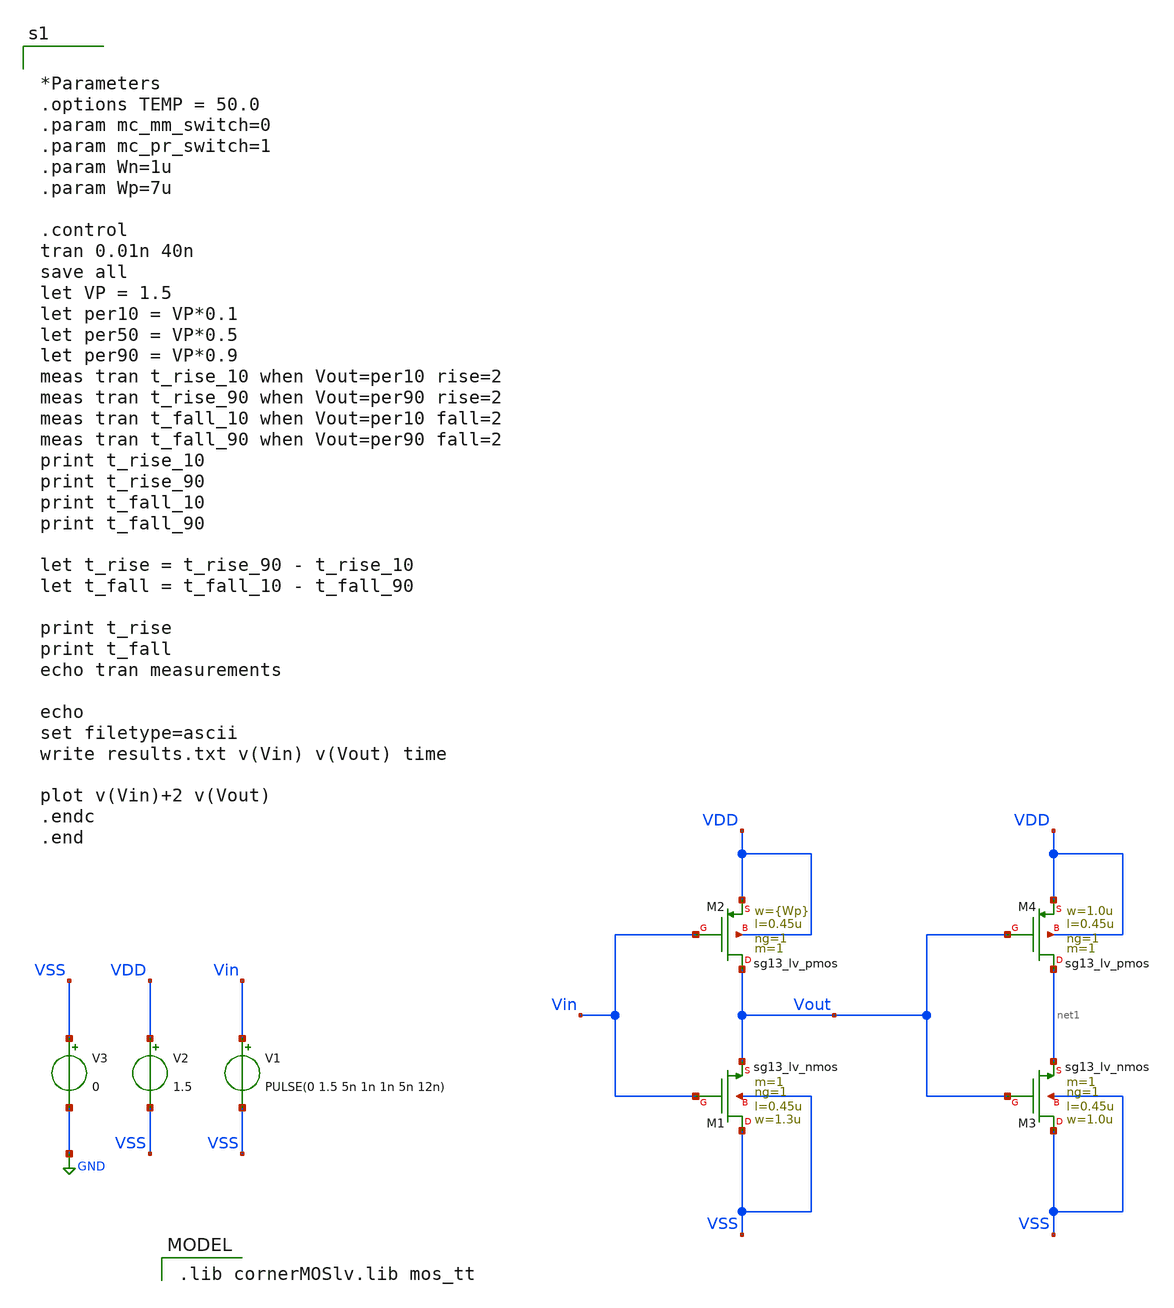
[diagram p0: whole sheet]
** sch_path: unic_cass_wrapper_user_project/ROs_reliability/inv_char.sch
**.subckt inv_char
XM1 VSS Vin Vout VSS sg13_lv_nmos w=1.3u l=0.45u ng=1 m=1 mm_ok=1
XM2 Vout Vin VDD VDD sg13_lv_pmos w={Wp} l=0.45u ng=1 m=1 mm_ok=1
XM3 VSS Vout net1 VSS sg13_lv_nmos w=1.0u l=0.45u ng=1 m=1 mm_ok=1
XM4 net1 Vout VDD VDD sg13_lv_pmos w=1.0u l=0.45u ng=1 m=1 mm_ok=1
V1 Vin VSS PULSE(0 1.5 5n 1n 1n 5n 12n)
V2 VDD VSS 1.5
V3 VSS GND 0
**** begin user architecture code
 .lib cornerMOSlv.lib mos_tt



*Parameters
.options TEMP = 50.0
.param mc_mm_switch=0
.param mc_pr_switch=1
.param Wn=1u
.param Wp=7u

.control
tran 0.01n 40n
save all
let VP = 1.5
let per10 = VP*0.1
let per50 = VP*0.5
let per90 = VP*0.9
meas tran t_rise_10 when Vout=per10 rise=2
meas tran t_rise_90 when Vout=per90 rise=2
meas tran t_fall_10 when Vout=per10 fall=2
meas tran t_fall_90 when Vout=per90 fall=2
print t_rise_10
print t_rise_90
print t_fall_10
print t_fall_90

let t_rise = t_rise_90 - t_rise_10
let t_fall = t_fall_10 - t_fall_90

print t_rise
print t_fall
echo tran measurements

echo
set filetype=ascii
write results.txt v(Vin) v(Vout) time

plot v(Vin)+2 v(Vout)
.endc
.end



**** end user architecture code
**.ends
.GLOBAL GND
.end
